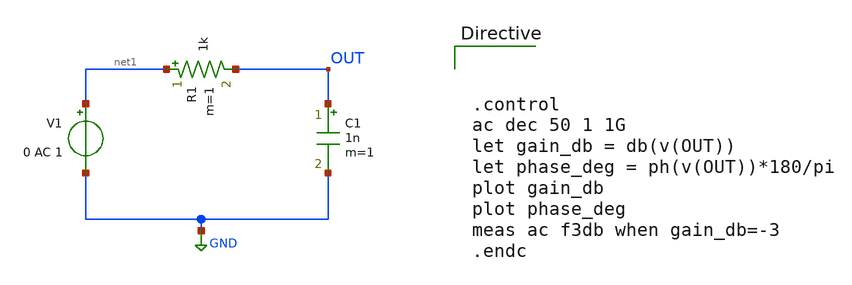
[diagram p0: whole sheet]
** sch_path: designs/sophiazhu/session_0/LPF.sch
**.subckt LPF
R1 net1 OUT 1k m=1
C1 OUT GND 1n m=1
V1 net1 GND 0 AC 1
**** begin user architecture code



.control
ac dec 50 1 1G
let gain_db = db(v(OUT))
let phase_deg = ph(v(OUT))*180/pi
plot gain_db
plot phase_deg
meas ac f3db when gain_db=-3
.endc



**** end user architecture code
**.ends
.GLOBAL GND
.end
